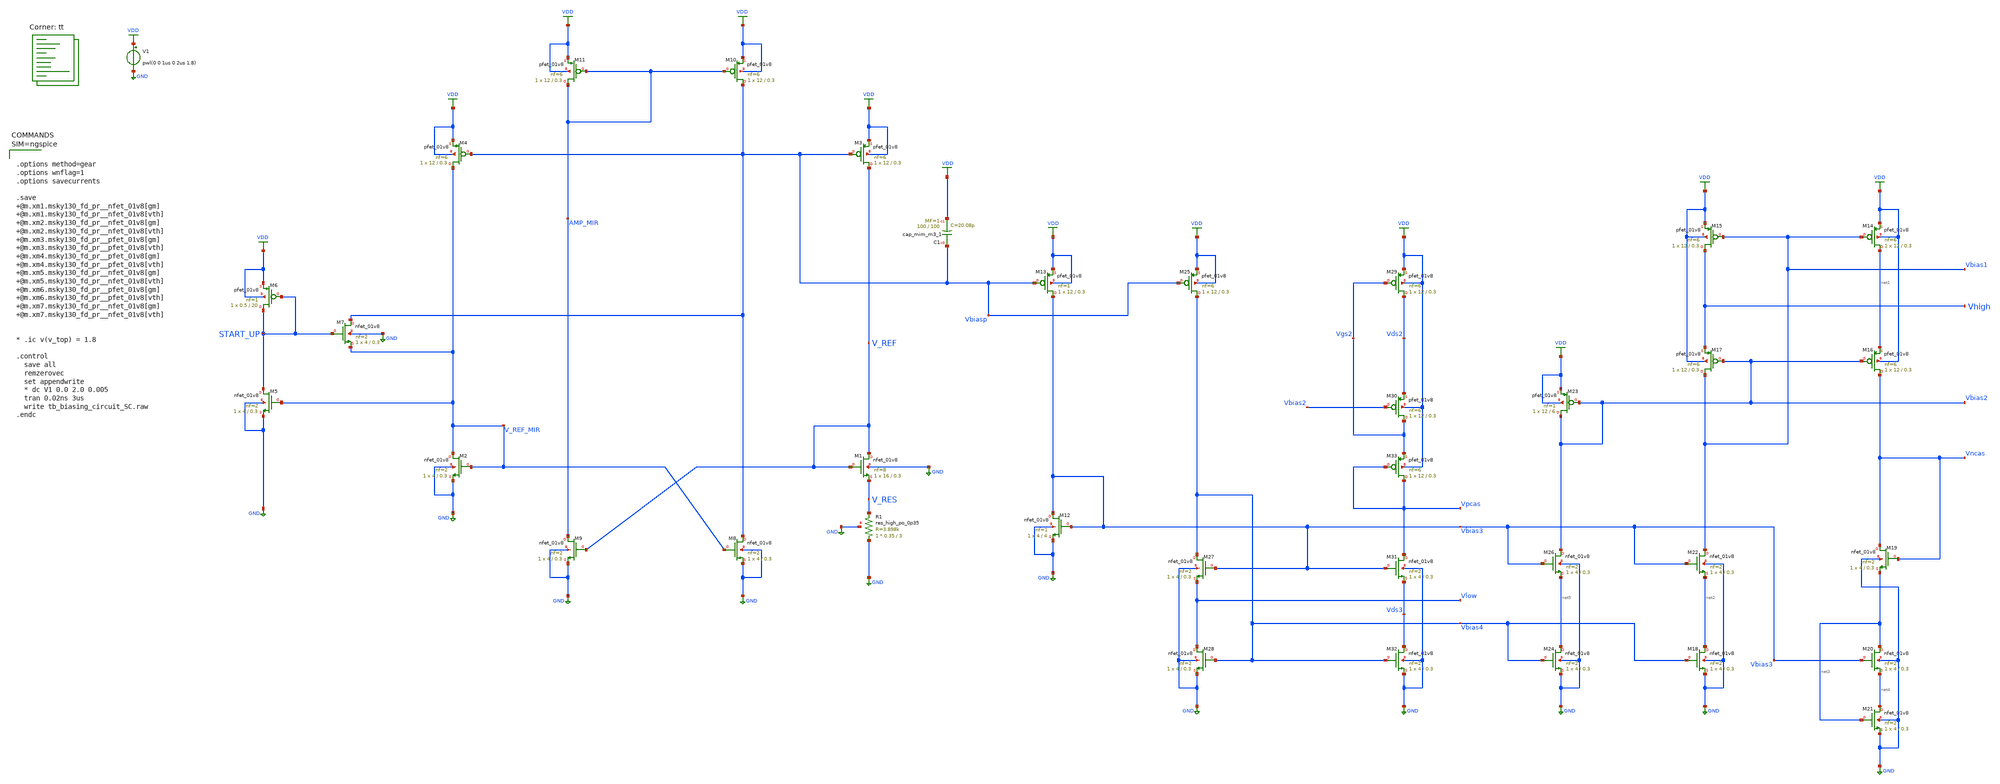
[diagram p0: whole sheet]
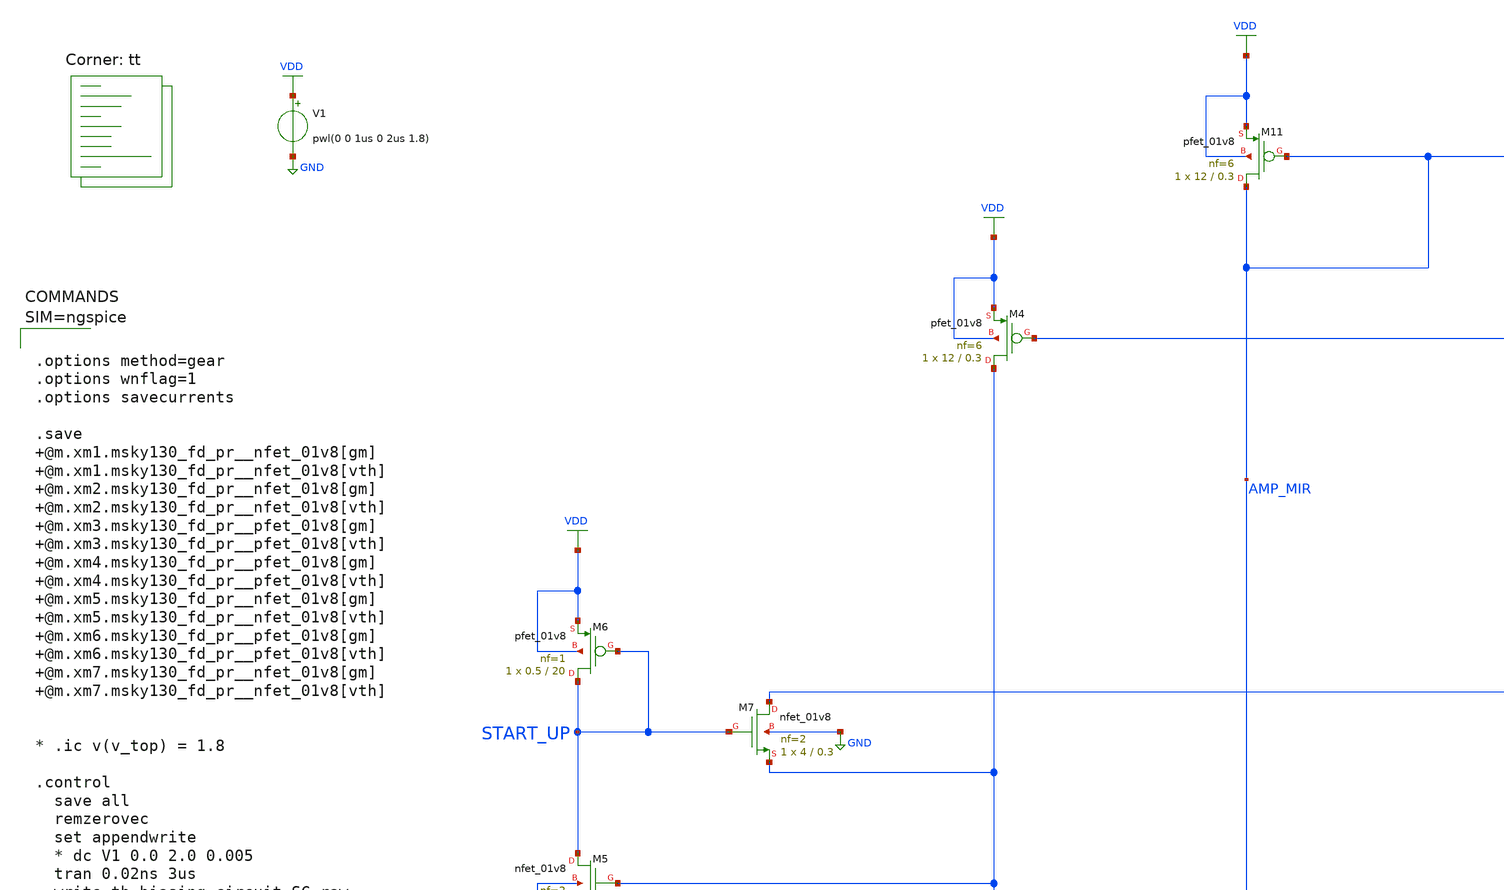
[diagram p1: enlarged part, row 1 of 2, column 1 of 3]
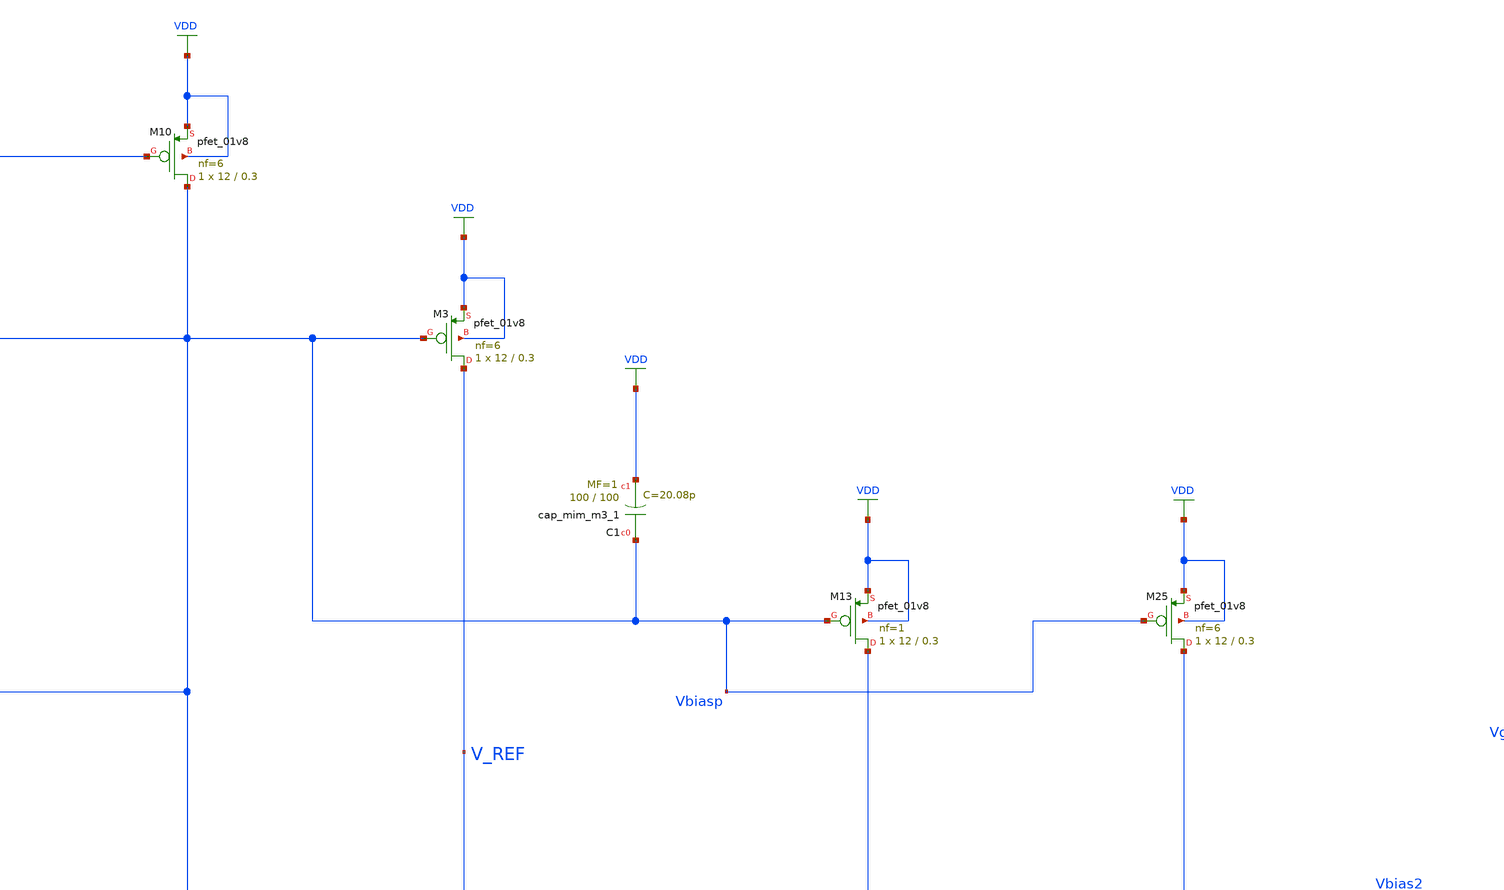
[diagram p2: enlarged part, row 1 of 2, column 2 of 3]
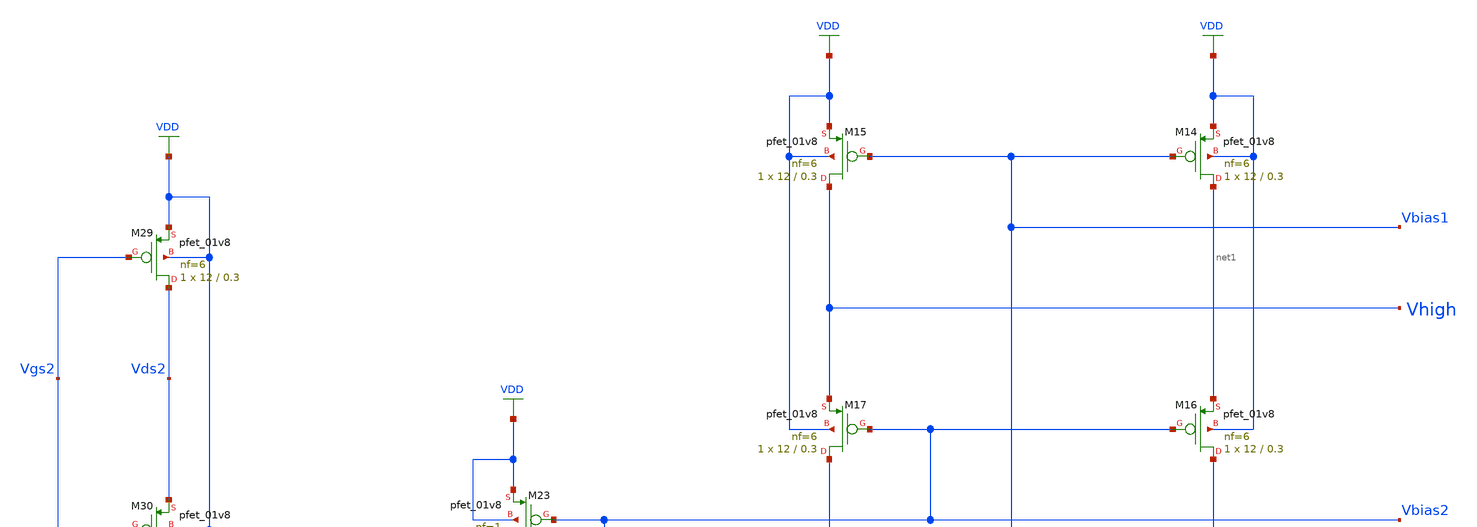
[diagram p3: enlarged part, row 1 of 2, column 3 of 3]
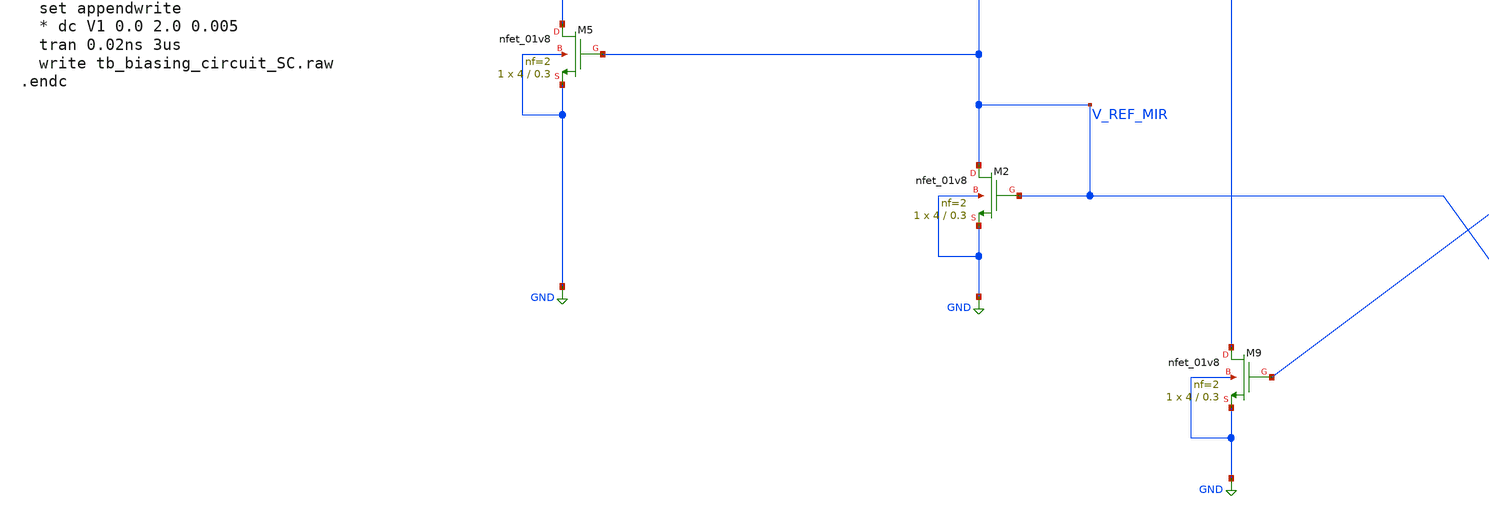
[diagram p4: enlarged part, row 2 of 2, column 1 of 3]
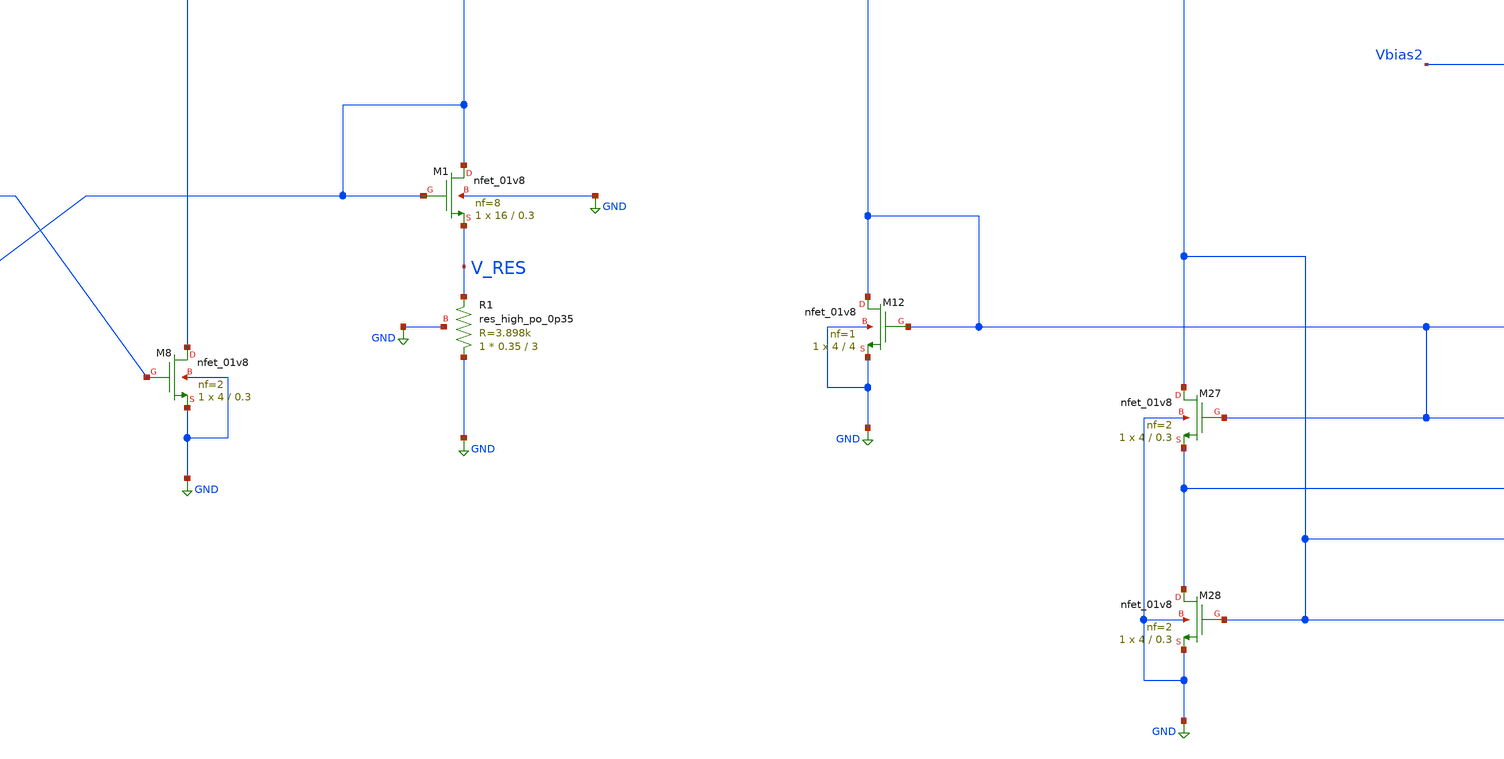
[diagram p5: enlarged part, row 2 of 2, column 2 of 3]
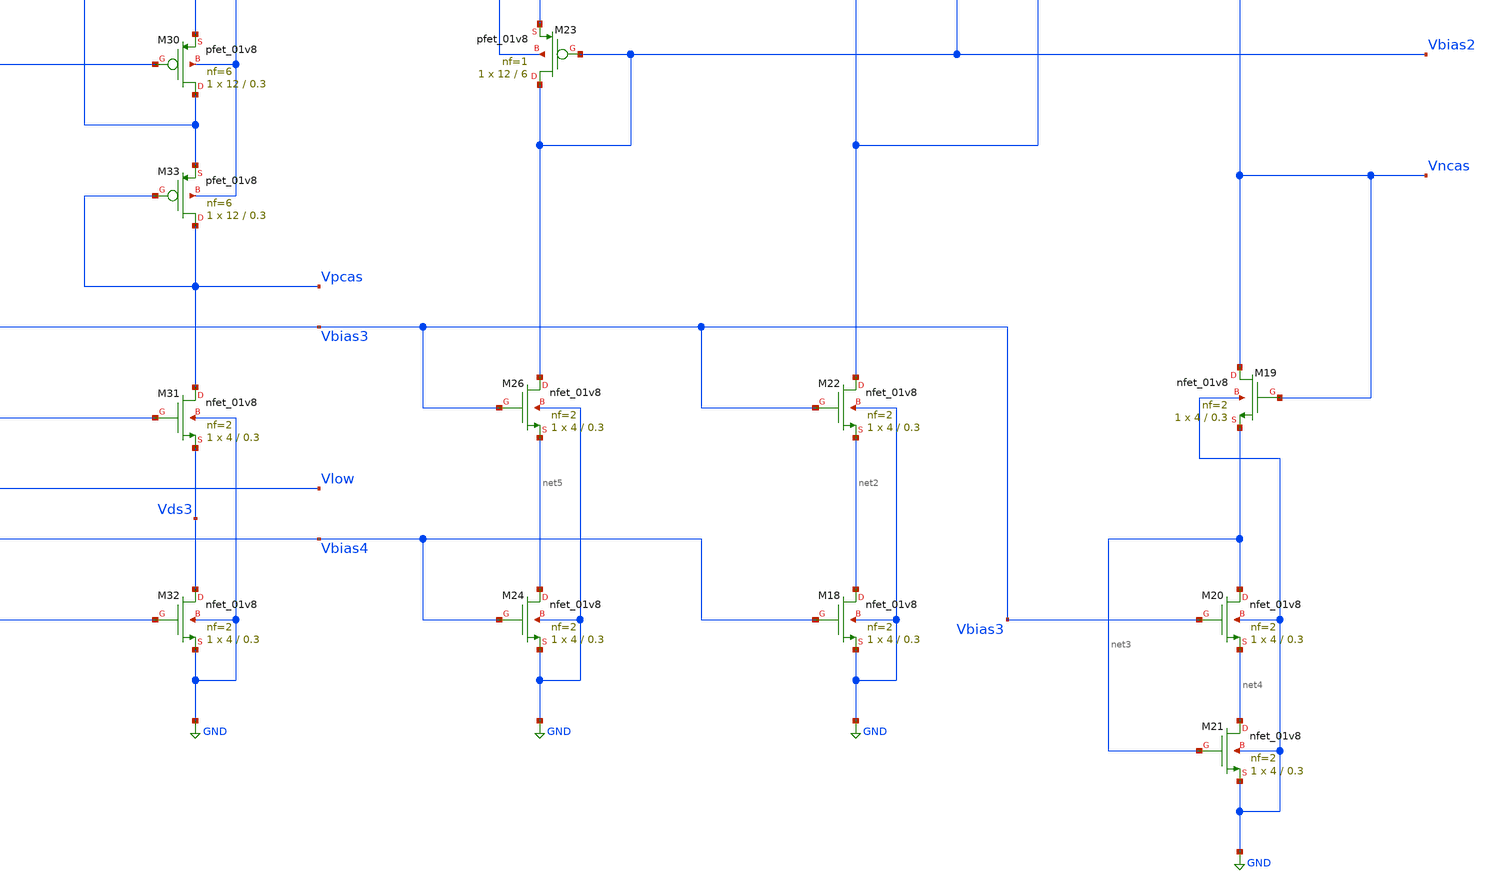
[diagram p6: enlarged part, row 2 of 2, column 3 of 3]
** sch_path: projects/ASU/EEE572/schematic/tb_biasing_circuit_SC.sch
**.subckt tb_biasing_circuit_SC
V1 VDD GND pwl(0 0 1us 0 2us 1.8)
XM1 V_REF V_REF V_RES GND sky130_fd_pr__nfet_01v8 L=0.3 W=16 nf=8 ad='int((nf+1)/2) * W/nf * 0.29' as='int((nf+2)/2) * W/nf * 0.29'
+ pd='2*int((nf+1)/2) * (W/nf + 0.29)' ps='2*int((nf+2)/2) * (W/nf + 0.29)' nrd='0.29 / W' nrs='0.29 / W'
+ sa=0 sb=0 sd=0 mult=1 m=1
XM2 V_REF_MIR V_REF_MIR GND GND sky130_fd_pr__nfet_01v8 L=0.3 W=4 nf=2 ad='int((nf+1)/2) * W/nf * 0.29'
+ as='int((nf+2)/2) * W/nf * 0.29' pd='2*int((nf+1)/2) * (W/nf + 0.29)' ps='2*int((nf+2)/2) * (W/nf + 0.29)'
+ nrd='0.29 / W' nrs='0.29 / W' sa=0 sb=0 sd=0 mult=1 m=1
XM5 START_UP V_REF_MIR GND GND sky130_fd_pr__nfet_01v8 L=0.3 W=4 nf=2 ad='int((nf+1)/2) * W/nf * 0.29'
+ as='int((nf+2)/2) * W/nf * 0.29' pd='2*int((nf+1)/2) * (W/nf + 0.29)' ps='2*int((nf+2)/2) * (W/nf + 0.29)'
+ nrd='0.29 / W' nrs='0.29 / W' sa=0 sb=0 sd=0 mult=1 m=1
XM7 Vbiasp START_UP V_REF_MIR GND sky130_fd_pr__nfet_01v8 L=0.3 W=4 nf=2 ad='int((nf+1)/2) * W/nf * 0.29'
+ as='int((nf+2)/2) * W/nf * 0.29' pd='2*int((nf+1)/2) * (W/nf + 0.29)' ps='2*int((nf+2)/2) * (W/nf + 0.29)'
+ nrd='0.29 / W' nrs='0.29 / W' sa=0 sb=0 sd=0 mult=1 m=1
XR1 GND V_RES GND sky130_fd_pr__res_high_po_0p35 L=3 mult=1 m=1
XM6 START_UP START_UP VDD VDD sky130_fd_pr__pfet_01v8 L=20 W=0.5 nf=1 ad='int((nf+1)/2) * W/nf * 0.29'
+ as='int((nf+2)/2) * W/nf * 0.29' pd='2*int((nf+1)/2) * (W/nf + 0.29)' ps='2*int((nf+2)/2) * (W/nf + 0.29)'
+ nrd='0.29 / W' nrs='0.29 / W' sa=0 sb=0 sd=0 mult=1 m=1
XM3 V_REF Vbiasp VDD VDD sky130_fd_pr__pfet_01v8 L=0.3 W=12 nf=6 ad='int((nf+1)/2) * W/nf * 0.29' as='int((nf+2)/2) * W/nf * 0.29'
+ pd='2*int((nf+1)/2) * (W/nf + 0.29)' ps='2*int((nf+2)/2) * (W/nf + 0.29)' nrd='0.29 / W' nrs='0.29 / W'
+ sa=0 sb=0 sd=0 mult=1 m=1
XM4 V_REF_MIR Vbiasp VDD VDD sky130_fd_pr__pfet_01v8 L=0.3 W=12 nf=6 ad='int((nf+1)/2) * W/nf * 0.29'
+ as='int((nf+2)/2) * W/nf * 0.29' pd='2*int((nf+1)/2) * (W/nf + 0.29)' ps='2*int((nf+2)/2) * (W/nf + 0.29)'
+ nrd='0.29 / W' nrs='0.29 / W' sa=0 sb=0 sd=0 mult=1 m=1
XM8 Vbiasp V_REF_MIR GND GND sky130_fd_pr__nfet_01v8 L=0.3 W=4 nf=2 ad='int((nf+1)/2) * W/nf * 0.29'
+ as='int((nf+2)/2) * W/nf * 0.29' pd='2*int((nf+1)/2) * (W/nf + 0.29)' ps='2*int((nf+2)/2) * (W/nf + 0.29)'
+ nrd='0.29 / W' nrs='0.29 / W' sa=0 sb=0 sd=0 mult=1 m=1
XM9 AMP_MIR V_REF GND GND sky130_fd_pr__nfet_01v8 L=0.3 W=4 nf=2 ad='int((nf+1)/2) * W/nf * 0.29' as='int((nf+2)/2) * W/nf * 0.29'
+ pd='2*int((nf+1)/2) * (W/nf + 0.29)' ps='2*int((nf+2)/2) * (W/nf + 0.29)' nrd='0.29 / W' nrs='0.29 / W'
+ sa=0 sb=0 sd=0 mult=1 m=1
XM10 Vbiasp AMP_MIR VDD VDD sky130_fd_pr__pfet_01v8 L=0.3 W=12 nf=6 ad='int((nf+1)/2) * W/nf * 0.29'
+ as='int((nf+2)/2) * W/nf * 0.29' pd='2*int((nf+1)/2) * (W/nf + 0.29)' ps='2*int((nf+2)/2) * (W/nf + 0.29)'
+ nrd='0.29 / W' nrs='0.29 / W' sa=0 sb=0 sd=0 mult=1 m=1
XM11 AMP_MIR AMP_MIR VDD VDD sky130_fd_pr__pfet_01v8 L=0.3 W=12 nf=6 ad='int((nf+1)/2) * W/nf * 0.29'
+ as='int((nf+2)/2) * W/nf * 0.29' pd='2*int((nf+1)/2) * (W/nf + 0.29)' ps='2*int((nf+2)/2) * (W/nf + 0.29)'
+ nrd='0.29 / W' nrs='0.29 / W' sa=0 sb=0 sd=0 mult=1 m=1
XM12 Vbias3 Vbias3 GND GND sky130_fd_pr__nfet_01v8 L=4 W=4 nf=1 ad='int((nf+1)/2) * W/nf * 0.29' as='int((nf+2)/2) * W/nf * 0.29'
+ pd='2*int((nf+1)/2) * (W/nf + 0.29)' ps='2*int((nf+2)/2) * (W/nf + 0.29)' nrd='0.29 / W' nrs='0.29 / W'
+ sa=0 sb=0 sd=0 mult=1 m=1
XM13 Vbias3 Vbiasp VDD VDD sky130_fd_pr__pfet_01v8 L=0.3 W=12 nf=1 ad='int((nf+1)/2) * W/nf * 0.29' as='int((nf+2)/2) * W/nf * 0.29'
+ pd='2*int((nf+1)/2) * (W/nf + 0.29)' ps='2*int((nf+2)/2) * (W/nf + 0.29)' nrd='0.29 / W' nrs='0.29 / W'
+ sa=0 sb=0 sd=0 mult=1 m=1
XM14 net1 Vbias1 VDD VDD sky130_fd_pr__pfet_01v8 L=0.3 W=12 nf=6 ad='int((nf+1)/2) * W/nf * 0.29' as='int((nf+2)/2) * W/nf * 0.29'
+ pd='2*int((nf+1)/2) * (W/nf + 0.29)' ps='2*int((nf+2)/2) * (W/nf + 0.29)' nrd='0.29 / W' nrs='0.29 / W'
+ sa=0 sb=0 sd=0 mult=1 m=1
XM15 Vhigh Vbias1 VDD VDD sky130_fd_pr__pfet_01v8 L=0.3 W=12 nf=6 ad='int((nf+1)/2) * W/nf * 0.29' as='int((nf+2)/2) * W/nf * 0.29'
+ pd='2*int((nf+1)/2) * (W/nf + 0.29)' ps='2*int((nf+2)/2) * (W/nf + 0.29)' nrd='0.29 / W' nrs='0.29 / W'
+ sa=0 sb=0 sd=0 mult=1 m=1
XM16 Vncas Vbias2 net1 VDD sky130_fd_pr__pfet_01v8 L=0.3 W=12 nf=6 ad='int((nf+1)/2) * W/nf * 0.29' as='int((nf+2)/2) * W/nf * 0.29'
+ pd='2*int((nf+1)/2) * (W/nf + 0.29)' ps='2*int((nf+2)/2) * (W/nf + 0.29)' nrd='0.29 / W' nrs='0.29 / W'
+ sa=0 sb=0 sd=0 mult=1 m=1
XM17 Vbias1 Vbias2 Vhigh VDD sky130_fd_pr__pfet_01v8 L=0.3 W=12 nf=6 ad='int((nf+1)/2) * W/nf * 0.29'
+ as='int((nf+2)/2) * W/nf * 0.29' pd='2*int((nf+1)/2) * (W/nf + 0.29)' ps='2*int((nf+2)/2) * (W/nf + 0.29)'
+ nrd='0.29 / W' nrs='0.29 / W' sa=0 sb=0 sd=0 mult=1 m=1
XM18 net2 Vbias4 GND GND sky130_fd_pr__nfet_01v8 L=0.3 W=4 nf=2 ad='int((nf+1)/2) * W/nf * 0.29' as='int((nf+2)/2) * W/nf * 0.29'
+ pd='2*int((nf+1)/2) * (W/nf + 0.29)' ps='2*int((nf+2)/2) * (W/nf + 0.29)' nrd='0.29 / W' nrs='0.29 / W'
+ sa=0 sb=0 sd=0 mult=1 m=1
XM19 Vncas Vncas net3 GND sky130_fd_pr__nfet_01v8 L=0.3 W=4 nf=2 ad='int((nf+1)/2) * W/nf * 0.29' as='int((nf+2)/2) * W/nf * 0.29'
+ pd='2*int((nf+1)/2) * (W/nf + 0.29)' ps='2*int((nf+2)/2) * (W/nf + 0.29)' nrd='0.29 / W' nrs='0.29 / W'
+ sa=0 sb=0 sd=0 mult=1 m=1
XM20 net3 Vbias3 net4 GND sky130_fd_pr__nfet_01v8 L=0.3 W=4 nf=2 ad='int((nf+1)/2) * W/nf * 0.29' as='int((nf+2)/2) * W/nf * 0.29'
+ pd='2*int((nf+1)/2) * (W/nf + 0.29)' ps='2*int((nf+2)/2) * (W/nf + 0.29)' nrd='0.29 / W' nrs='0.29 / W'
+ sa=0 sb=0 sd=0 mult=1 m=1
XM21 net4 net3 GND GND sky130_fd_pr__nfet_01v8 L=0.3 W=4 nf=2 ad='int((nf+1)/2) * W/nf * 0.29' as='int((nf+2)/2) * W/nf * 0.29'
+ pd='2*int((nf+1)/2) * (W/nf + 0.29)' ps='2*int((nf+2)/2) * (W/nf + 0.29)' nrd='0.29 / W' nrs='0.29 / W'
+ sa=0 sb=0 sd=0 mult=1 m=1
XM25 Vbias4 Vbiasp VDD VDD sky130_fd_pr__pfet_01v8 L=0.3 W=12 nf=6 ad='int((nf+1)/2) * W/nf * 0.29' as='int((nf+2)/2) * W/nf * 0.29'
+ pd='2*int((nf+1)/2) * (W/nf + 0.29)' ps='2*int((nf+2)/2) * (W/nf + 0.29)' nrd='0.29 / W' nrs='0.29 / W'
+ sa=0 sb=0 sd=0 mult=1 m=1
XM27 Vbias4 Vbias3 Vlow GND sky130_fd_pr__nfet_01v8 L=0.3 W=4 nf=2 ad='int((nf+1)/2) * W/nf * 0.29' as='int((nf+2)/2) * W/nf * 0.29'
+ pd='2*int((nf+1)/2) * (W/nf + 0.29)' ps='2*int((nf+2)/2) * (W/nf + 0.29)' nrd='0.29 / W' nrs='0.29 / W'
+ sa=0 sb=0 sd=0 mult=1 m=1
XM28 Vlow Vbias4 GND GND sky130_fd_pr__nfet_01v8 L=0.3 W=4 nf=2 ad='int((nf+1)/2) * W/nf * 0.29' as='int((nf+2)/2) * W/nf * 0.29'
+ pd='2*int((nf+1)/2) * (W/nf + 0.29)' ps='2*int((nf+2)/2) * (W/nf + 0.29)' nrd='0.29 / W' nrs='0.29 / W'
+ sa=0 sb=0 sd=0 mult=1 m=1
XM29 Vds2 Vgs2 VDD VDD sky130_fd_pr__pfet_01v8 L=0.3 W=12 nf=6 ad='int((nf+1)/2) * W/nf * 0.29' as='int((nf+2)/2) * W/nf * 0.29'
+ pd='2*int((nf+1)/2) * (W/nf + 0.29)' ps='2*int((nf+2)/2) * (W/nf + 0.29)' nrd='0.29 / W' nrs='0.29 / W'
+ sa=0 sb=0 sd=0 mult=1 m=1
XM30 Vgs2 Vbias2 Vds2 VDD sky130_fd_pr__pfet_01v8 L=0.3 W=12 nf=6 ad='int((nf+1)/2) * W/nf * 0.29' as='int((nf+2)/2) * W/nf * 0.29'
+ pd='2*int((nf+1)/2) * (W/nf + 0.29)' ps='2*int((nf+2)/2) * (W/nf + 0.29)' nrd='0.29 / W' nrs='0.29 / W'
+ sa=0 sb=0 sd=0 mult=1 m=1
XM31 Vpcas Vbias3 Vds3 GND sky130_fd_pr__nfet_01v8 L=0.3 W=4 nf=2 ad='int((nf+1)/2) * W/nf * 0.29' as='int((nf+2)/2) * W/nf * 0.29'
+ pd='2*int((nf+1)/2) * (W/nf + 0.29)' ps='2*int((nf+2)/2) * (W/nf + 0.29)' nrd='0.29 / W' nrs='0.29 / W'
+ sa=0 sb=0 sd=0 mult=1 m=1
XM32 Vds3 Vbias4 GND GND sky130_fd_pr__nfet_01v8 L=0.3 W=4 nf=2 ad='int((nf+1)/2) * W/nf * 0.29' as='int((nf+2)/2) * W/nf * 0.29'
+ pd='2*int((nf+1)/2) * (W/nf + 0.29)' ps='2*int((nf+2)/2) * (W/nf + 0.29)' nrd='0.29 / W' nrs='0.29 / W'
+ sa=0 sb=0 sd=0 mult=1 m=1
XM33 Vpcas Vpcas Vgs2 VDD sky130_fd_pr__pfet_01v8 L=0.3 W=12 nf=6 ad='int((nf+1)/2) * W/nf * 0.29' as='int((nf+2)/2) * W/nf * 0.29'
+ pd='2*int((nf+1)/2) * (W/nf + 0.29)' ps='2*int((nf+2)/2) * (W/nf + 0.29)' nrd='0.29 / W' nrs='0.29 / W'
+ sa=0 sb=0 sd=0 mult=1 m=1
XM22 Vbias1 Vbias3 net2 GND sky130_fd_pr__nfet_01v8 L=0.3 W=4 nf=2 ad='int((nf+1)/2) * W/nf * 0.29' as='int((nf+2)/2) * W/nf * 0.29'
+ pd='2*int((nf+1)/2) * (W/nf + 0.29)' ps='2*int((nf+2)/2) * (W/nf + 0.29)' nrd='0.29 / W' nrs='0.29 / W'
+ sa=0 sb=0 sd=0 mult=1 m=1
XM23 Vbias2 Vbias2 VDD VDD sky130_fd_pr__pfet_01v8 L=6 W=12 nf=1 ad='int((nf+1)/2) * W/nf * 0.29' as='int((nf+2)/2) * W/nf * 0.29'
+ pd='2*int((nf+1)/2) * (W/nf + 0.29)' ps='2*int((nf+2)/2) * (W/nf + 0.29)' nrd='0.29 / W' nrs='0.29 / W'
+ sa=0 sb=0 sd=0 mult=1 m=1
XM24 net5 Vbias4 GND GND sky130_fd_pr__nfet_01v8 L=0.3 W=4 nf=2 ad='int((nf+1)/2) * W/nf * 0.29' as='int((nf+2)/2) * W/nf * 0.29'
+ pd='2*int((nf+1)/2) * (W/nf + 0.29)' ps='2*int((nf+2)/2) * (W/nf + 0.29)' nrd='0.29 / W' nrs='0.29 / W'
+ sa=0 sb=0 sd=0 mult=1 m=1
XM26 Vbias2 Vbias3 net5 GND sky130_fd_pr__nfet_01v8 L=0.3 W=4 nf=2 ad='int((nf+1)/2) * W/nf * 0.29' as='int((nf+2)/2) * W/nf * 0.29'
+ pd='2*int((nf+1)/2) * (W/nf + 0.29)' ps='2*int((nf+2)/2) * (W/nf + 0.29)' nrd='0.29 / W' nrs='0.29 / W'
+ sa=0 sb=0 sd=0 mult=1 m=1
XC1 Vbiasp VDD sky130_fd_pr__cap_mim_m3_1 W=100 L=100 MF=1 m=1
**** begin user architecture code
.lib $::SKYWATER_MODELS/sky130.lib.spice tt



.options method=gear
.options wnflag=1
.options savecurrents

.save @m.xm1.msky130_fd_pr__nfet_01v8[gm] @m.xm1.msky130_fd_pr__nfet_01v8[vth] @m.xm2.msky130_fd_pr__nfet_01v8[gm] @m.xm2.msky130_fd_pr__nfet_01v8[vth] @m.xm3.msky130_fd_pr__pfet_01v8[gm] @m.xm3.msky130_fd_pr__pfet_01v8[vth] @m.xm4.msky130_fd_pr__pfet_01v8[gm] @m.xm4.msky130_fd_pr__pfet_01v8[vth] @m.xm5.msky130_fd_pr__nfet_01v8[gm] @m.xm5.msky130_fd_pr__nfet_01v8[vth] @m.xm6.msky130_fd_pr__pfet_01v8[gm] @m.xm6.msky130_fd_pr__pfet_01v8[vth] @m.xm7.msky130_fd_pr__nfet_01v8[gm] @m.xm7.msky130_fd_pr__nfet_01v8[vth]


* .ic v(v_top) = 1.8

.control
  save all
  remzerovec
  set appendwrite
  * dc V1 0.0 2.0 0.005
  tran 0.02ns 3us
  write tb_biasing_circuit_SC.raw
.endc





**** end user architecture code
**.ends
.GLOBAL GND
.GLOBAL VDD
.end
